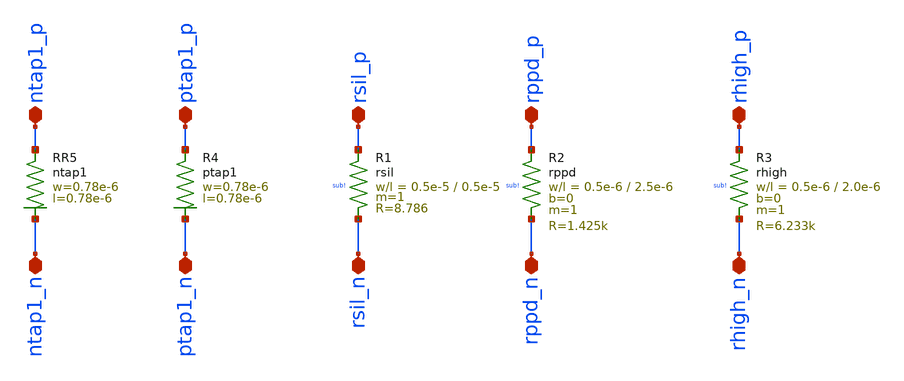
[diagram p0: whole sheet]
** sch_path: ts_pr_May2024/design_data/xschem/resistors.sch
**.subckt resistors ntap1_p ptap1_p rsil_p rppd_p rhigh_p ntap1_n ptap1_n rsil_n rppd_n rhigh_n
*.iopin ntap1_p
*.iopin ptap1_p
*.iopin rsil_p
*.iopin rppd_p
*.iopin rhigh_p
*.iopin ntap1_n
*.iopin ptap1_n
*.iopin rsil_n
*.iopin rppd_n
*.iopin rhigh_n
XR2 rppd_p rppd_n sub! rppd w=0.5e-6 l=2.5e-6 m=1 b=0 mm_ok=1
XR3 rhigh_p rhigh_n sub! rhigh w=0.5e-6 l=2.0e-6 m=1 b=0 mm_ok=1
XR1 rsil_p rsil_n sub! rsil w=0.5e-5 l=0.5e-5 m=1 mm_ok=1
XR4 ptap1_p ptap1_n ptap1 R=262.8 w=0.78e-6 l=0.78e-6
XR5 ntap1_p ntap1_n ntap1 R=262.8 w=0.78e-6 l=0.78e-6
**.ends
.end
